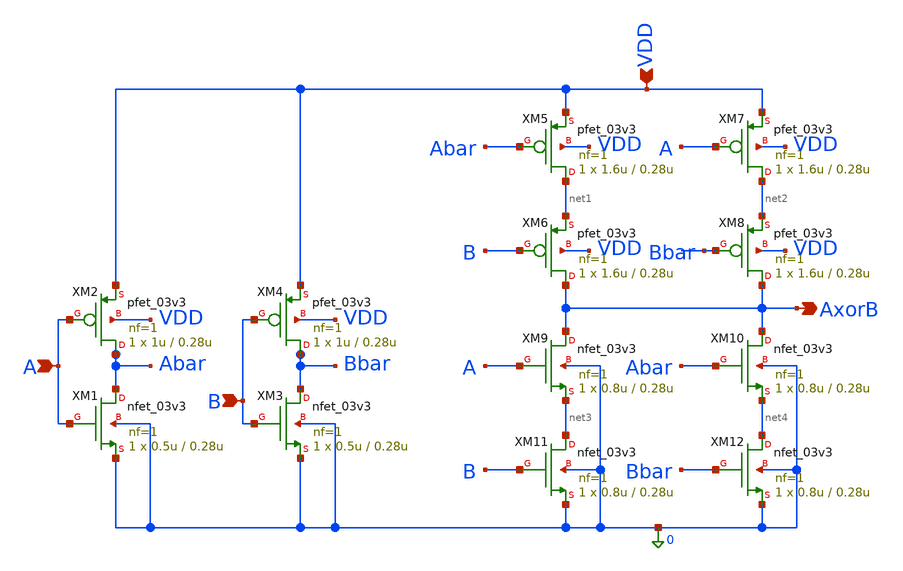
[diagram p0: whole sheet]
** sch_path: Design_Files/IC Design/Schematic/SAR_ADC_BLOCKS/XOR/XOR.sch
**.subckt XOR VDD A B AxorB
*.ipin VDD
*.ipin A
*.ipin B
*.opin AxorB
XM1 Abar A 0 0 nfet_03v3 L=0.28u W=0.5u nf=1 ad='int((nf+1)/2) * W/nf * 0.18u' as='int((nf+2)/2) * W/nf * 0.18u'
+ pd='2*int((nf+1)/2) * (W/nf + 0.18u)' ps='2*int((nf+2)/2) * (W/nf + 0.18u)' nrd='0.18u / W' nrs='0.18u / W'
+ sa=0 sb=0 sd=0 m=1
XM2 Abar A VDD VDD pfet_03v3 L=0.28u W=1u nf=1 ad='int((nf+1)/2) * W/nf * 0.18u' as='int((nf+2)/2) * W/nf * 0.18u'
+ pd='2*int((nf+1)/2) * (W/nf + 0.18u)' ps='2*int((nf+2)/2) * (W/nf + 0.18u)' nrd='0.18u / W' nrs='0.18u / W'
+ sa=0 sb=0 sd=0 m=1
XM3 Bbar B 0 0 nfet_03v3 L=0.28u W=0.5u nf=1 ad='int((nf+1)/2) * W/nf * 0.18u' as='int((nf+2)/2) * W/nf * 0.18u'
+ pd='2*int((nf+1)/2) * (W/nf + 0.18u)' ps='2*int((nf+2)/2) * (W/nf + 0.18u)' nrd='0.18u / W' nrs='0.18u / W'
+ sa=0 sb=0 sd=0 m=1
XM4 Bbar B VDD VDD pfet_03v3 L=0.28u W=1u nf=1 ad='int((nf+1)/2) * W/nf * 0.18u' as='int((nf+2)/2) * W/nf * 0.18u'
+ pd='2*int((nf+1)/2) * (W/nf + 0.18u)' ps='2*int((nf+2)/2) * (W/nf + 0.18u)' nrd='0.18u / W' nrs='0.18u / W'
+ sa=0 sb=0 sd=0 m=1
XM5 net1 Abar VDD VDD pfet_03v3 L=0.28u W=1.6u nf=1 ad='int((nf+1)/2) * W/nf * 0.18u' as='int((nf+2)/2) * W/nf * 0.18u'
+ pd='2*int((nf+1)/2) * (W/nf + 0.18u)' ps='2*int((nf+2)/2) * (W/nf + 0.18u)' nrd='0.18u / W' nrs='0.18u / W'
+ sa=0 sb=0 sd=0 m=1
XM6 AxorB B net1 VDD pfet_03v3 L=0.28u W=1.6u nf=1 ad='int((nf+1)/2) * W/nf * 0.18u' as='int((nf+2)/2) * W/nf * 0.18u'
+ pd='2*int((nf+1)/2) * (W/nf + 0.18u)' ps='2*int((nf+2)/2) * (W/nf + 0.18u)' nrd='0.18u / W' nrs='0.18u / W'
+ sa=0 sb=0 sd=0 m=1
XM7 net2 A VDD VDD pfet_03v3 L=0.28u W=1.6u nf=1 ad='int((nf+1)/2) * W/nf * 0.18u' as='int((nf+2)/2) * W/nf * 0.18u'
+ pd='2*int((nf+1)/2) * (W/nf + 0.18u)' ps='2*int((nf+2)/2) * (W/nf + 0.18u)' nrd='0.18u / W' nrs='0.18u / W'
+ sa=0 sb=0 sd=0 m=1
XM8 AxorB Bbar net2 VDD pfet_03v3 L=0.28u W=1.6u nf=1 ad='int((nf+1)/2) * W/nf * 0.18u' as='int((nf+2)/2) * W/nf * 0.18u'
+ pd='2*int((nf+1)/2) * (W/nf + 0.18u)' ps='2*int((nf+2)/2) * (W/nf + 0.18u)' nrd='0.18u / W' nrs='0.18u / W'
+ sa=0 sb=0 sd=0 m=1
XM9 AxorB A net3 0 nfet_03v3 L=0.28u W=0.8u nf=1 ad='int((nf+1)/2) * W/nf * 0.18u' as='int((nf+2)/2) * W/nf * 0.18u'
+ pd='2*int((nf+1)/2) * (W/nf + 0.18u)' ps='2*int((nf+2)/2) * (W/nf + 0.18u)' nrd='0.18u / W' nrs='0.18u / W'
+ sa=0 sb=0 sd=0 m=1
XM10 AxorB Abar net4 0 nfet_03v3 L=0.28u W=0.8u nf=1 ad='int((nf+1)/2) * W/nf * 0.18u' as='int((nf+2)/2) * W/nf * 0.18u'
+ pd='2*int((nf+1)/2) * (W/nf + 0.18u)' ps='2*int((nf+2)/2) * (W/nf + 0.18u)' nrd='0.18u / W' nrs='0.18u / W'
+ sa=0 sb=0 sd=0 m=1
XM11 net3 B 0 0 nfet_03v3 L=0.28u W=0.8u nf=1 ad='int((nf+1)/2) * W/nf * 0.18u' as='int((nf+2)/2) * W/nf * 0.18u'
+ pd='2*int((nf+1)/2) * (W/nf + 0.18u)' ps='2*int((nf+2)/2) * (W/nf + 0.18u)' nrd='0.18u / W' nrs='0.18u / W'
+ sa=0 sb=0 sd=0 m=1
XM12 net4 Bbar 0 0 nfet_03v3 L=0.28u W=0.8u nf=1 ad='int((nf+1)/2) * W/nf * 0.18u' as='int((nf+2)/2) * W/nf * 0.18u'
+ pd='2*int((nf+1)/2) * (W/nf + 0.18u)' ps='2*int((nf+2)/2) * (W/nf + 0.18u)' nrd='0.18u / W' nrs='0.18u / W'
+ sa=0 sb=0 sd=0 m=1
**.ends
.end
